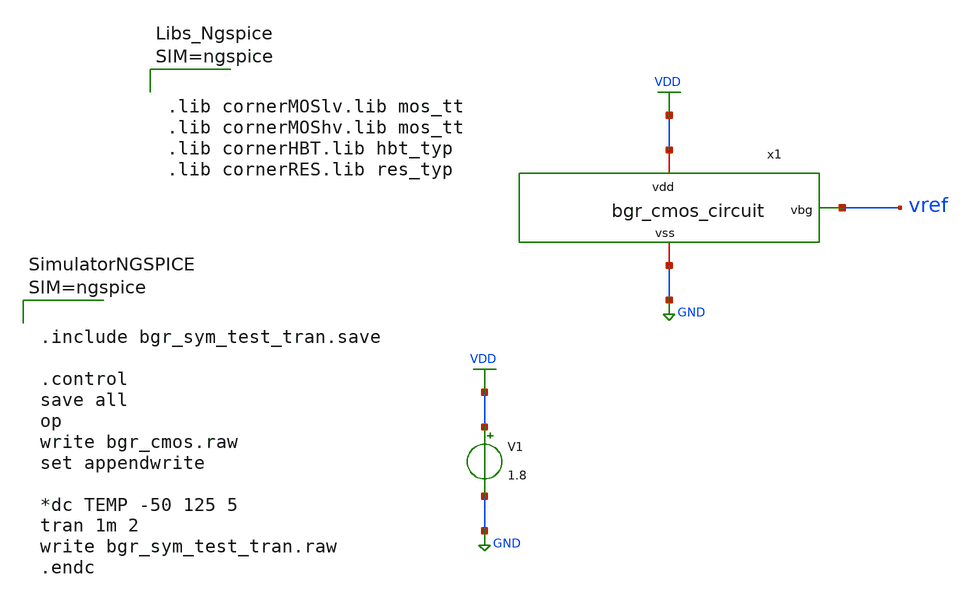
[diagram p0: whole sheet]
** sch_path: Schematics/ali_designs/bgr_sym_test_tran.sch
**.subckt bgr_sym_test_tran
x1 VDD GND vref bgr_cmos_circuit
V1 VDD GND 1.8
**** begin user architecture code



.include bgr_sym_test_tran.save

.control
save all
op
write bgr_cmos.raw
set appendwrite

*dc TEMP -50 125 5
tran 1m 2
write bgr_sym_test_tran.raw
.endc






.lib cornerMOSlv.lib mos_tt
.lib cornerMOShv.lib mos_tt
.lib cornerHBT.lib hbt_typ
.lib cornerRES.lib res_typ



**** end user architecture code
**.ends
.GLOBAL VDD
.GLOBAL GND
.end
